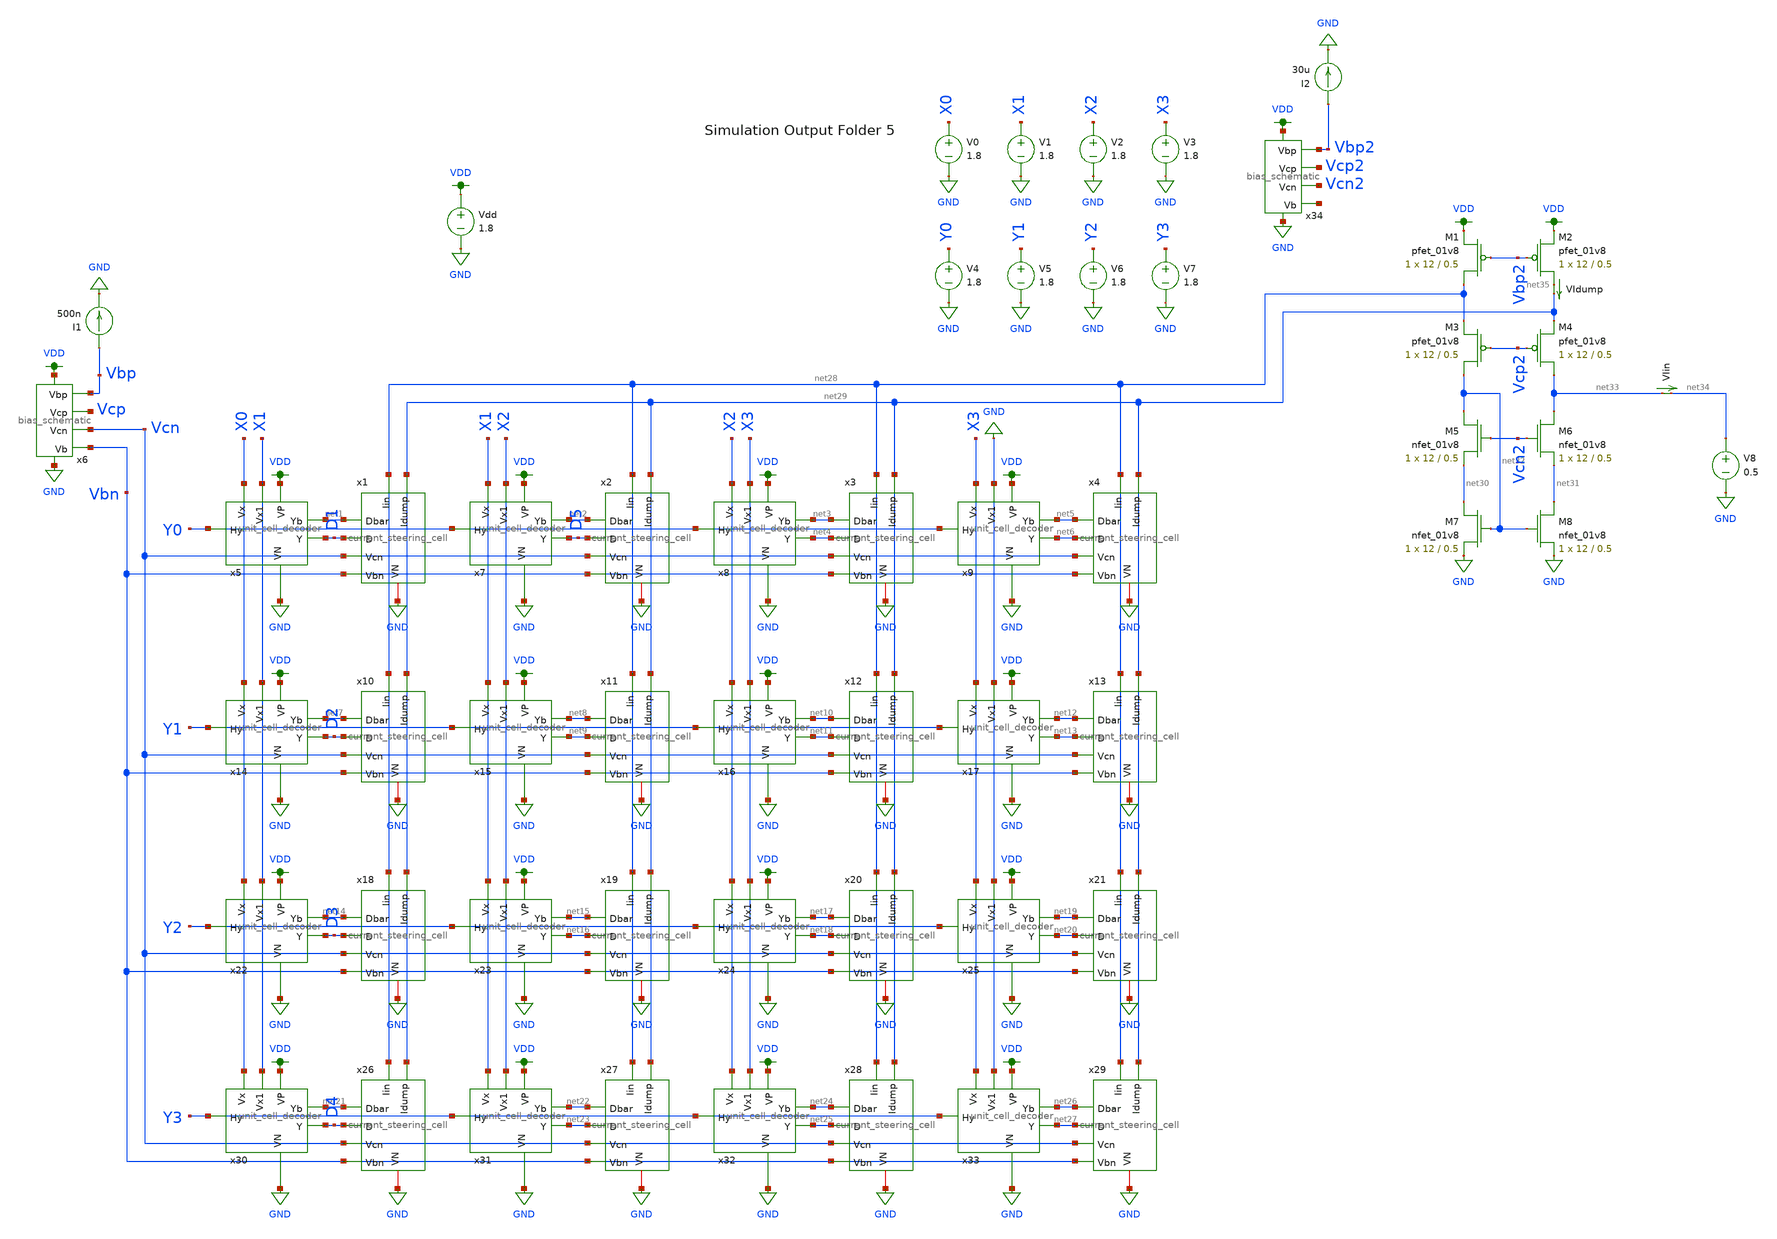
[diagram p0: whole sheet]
** sch_path: xschem/current_steering_testbenches/current_steering_testbench_current_difference.sch
**.subckt current_steering_testbench_current_difference
V1 X1 GND 1.8
V2 X2 GND 1.8
V3 X3 GND 1.8
V4 Y0 GND 1.8
I1 Vbp GND 500n
VIin net33 net34 0
.save i(viin)
Vdd VDD GND 1.8
XM1 net28 Vbp2 VDD VDD sky130_fd_pr__pfet_01v8 L=0.5 W=12 nf=1 ad='int((nf+1)/2) * W/nf * 0.29' as='int((nf+2)/2) * W/nf * 0.29'
+ pd='2*int((nf+1)/2) * (W/nf + 0.29)' ps='2*int((nf+2)/2) * (W/nf + 0.29)' nrd='0.29 / W' nrs='0.29 / W'
+ sa=0 sb=0 sd=0 mult=1 m=1
XM2 net35 Vbp2 VDD VDD sky130_fd_pr__pfet_01v8 L=0.5 W=12 nf=1 ad='int((nf+1)/2) * W/nf * 0.29' as='int((nf+2)/2) * W/nf * 0.29'
+ pd='2*int((nf+1)/2) * (W/nf + 0.29)' ps='2*int((nf+2)/2) * (W/nf + 0.29)' nrd='0.29 / W' nrs='0.29 / W'
+ sa=0 sb=0 sd=0 mult=1 m=1
XM3 net32 Vcp2 net28 VDD sky130_fd_pr__pfet_01v8 L=0.5 W=12 nf=1 ad='int((nf+1)/2) * W/nf * 0.29' as='int((nf+2)/2) * W/nf * 0.29'
+ pd='2*int((nf+1)/2) * (W/nf + 0.29)' ps='2*int((nf+2)/2) * (W/nf + 0.29)' nrd='0.29 / W' nrs='0.29 / W'
+ sa=0 sb=0 sd=0 mult=1 m=1
XM4 net33 Vcp2 net29 VDD sky130_fd_pr__pfet_01v8 L=0.5 W=12 nf=1 ad='int((nf+1)/2) * W/nf * 0.29' as='int((nf+2)/2) * W/nf * 0.29'
+ pd='2*int((nf+1)/2) * (W/nf + 0.29)' ps='2*int((nf+2)/2) * (W/nf + 0.29)' nrd='0.29 / W' nrs='0.29 / W'
+ sa=0 sb=0 sd=0 mult=1 m=1
V5 Y1 GND 1.8
V6 Y2 GND 1.8
V7 Y3 GND 1.8
V0 X0 GND 1.8
x5 X0 X1 Y0 VDD GND net1 D1 unit_cell_decoder
x7 X1 X2 Y0 VDD GND net2 D5 unit_cell_decoder
x8 X2 X3 Y0 VDD GND net3 net4 unit_cell_decoder
x9 X3 GND Y0 VDD GND net5 net6 unit_cell_decoder
x14 X0 X1 Y1 VDD GND net7 D2 unit_cell_decoder
x15 X1 X2 Y1 VDD GND net8 net9 unit_cell_decoder
x16 X2 X3 Y1 VDD GND net10 net11 unit_cell_decoder
x17 X3 GND Y1 VDD GND net12 net13 unit_cell_decoder
x22 X0 X1 Y2 VDD GND net14 D3 unit_cell_decoder
x23 X1 X2 Y2 VDD GND net15 net16 unit_cell_decoder
x24 X2 X3 Y2 VDD GND net17 net18 unit_cell_decoder
x25 X3 GND Y2 VDD GND net19 net20 unit_cell_decoder
x30 X0 X1 Y3 VDD GND net21 D4 unit_cell_decoder
x31 X1 X2 Y3 VDD GND net22 net23 unit_cell_decoder
x32 X2 X3 Y3 VDD GND net24 net25 unit_cell_decoder
x33 X3 GND Y3 VDD GND net26 net27 unit_cell_decoder
x1 net28 net29 net1 D1 Vcn Vbn GND current_steering_cell
x2 net28 net29 net2 D5 Vcn Vbn GND current_steering_cell
x3 net28 net29 net3 net4 Vcn Vbn GND current_steering_cell
x4 net28 net29 net5 net6 Vcn Vbn GND current_steering_cell
x10 net28 net29 net7 D2 Vcn Vbn GND current_steering_cell
x11 net28 net29 net8 net9 Vcn Vbn GND current_steering_cell
x12 net28 net29 net10 net11 Vcn Vbn GND current_steering_cell
x13 net28 net29 net12 net13 Vcn Vbn GND current_steering_cell
x18 net28 net29 net14 D3 Vcn Vbn GND current_steering_cell
x19 net28 net29 net15 net16 Vcn Vbn GND current_steering_cell
x20 net28 net29 net17 net18 Vcn Vbn GND current_steering_cell
x21 net28 net29 net19 net20 Vcn Vbn GND current_steering_cell
x26 net28 net29 net21 D4 Vcn Vbn GND current_steering_cell
x27 net28 net29 net22 net23 Vcn Vbn GND current_steering_cell
x28 net28 net29 net24 net25 Vcn Vbn GND current_steering_cell
x29 net28 net29 net26 net27 Vcn Vbn GND current_steering_cell
x6 VDD Vbp Vcp Vcn GND Vbn bias_schematic
XM5 net32 Vcn2 net30 GND sky130_fd_pr__nfet_01v8 L=0.5 W=12 nf=1 ad='int((nf+1)/2) * W/nf * 0.29' as='int((nf+2)/2) * W/nf * 0.29'
+ pd='2*int((nf+1)/2) * (W/nf + 0.29)' ps='2*int((nf+2)/2) * (W/nf + 0.29)' nrd='0.29 / W' nrs='0.29 / W'
+ sa=0 sb=0 sd=0 mult=1 m=1
XM6 net33 Vcn2 net31 GND sky130_fd_pr__nfet_01v8 L=0.5 W=12 nf=1 ad='int((nf+1)/2) * W/nf * 0.29' as='int((nf+2)/2) * W/nf * 0.29'
+ pd='2*int((nf+1)/2) * (W/nf + 0.29)' ps='2*int((nf+2)/2) * (W/nf + 0.29)' nrd='0.29 / W' nrs='0.29 / W'
+ sa=0 sb=0 sd=0 mult=1 m=1
XM7 net30 net32 GND GND sky130_fd_pr__nfet_01v8 L=0.5 W=12 nf=1 ad='int((nf+1)/2) * W/nf * 0.29' as='int((nf+2)/2) * W/nf * 0.29'
+ pd='2*int((nf+1)/2) * (W/nf + 0.29)' ps='2*int((nf+2)/2) * (W/nf + 0.29)' nrd='0.29 / W' nrs='0.29 / W'
+ sa=0 sb=0 sd=0 mult=1 m=1
XM8 net31 net32 GND GND sky130_fd_pr__nfet_01v8 L=0.5 W=12 nf=1 ad='int((nf+1)/2) * W/nf * 0.29' as='int((nf+2)/2) * W/nf * 0.29'
+ pd='2*int((nf+1)/2) * (W/nf + 0.29)' ps='2*int((nf+2)/2) * (W/nf + 0.29)' nrd='0.29 / W' nrs='0.29 / W'
+ sa=0 sb=0 sd=0 mult=1 m=1
V8 net34 GND 0.5
VIdump net35 net29 0
.save i(vidump)
I2 Vbp2 GND 30u
x34 VDD Vbp2 Vcp2 Vcn2 GND net36 bias_schematic
**** begin user architecture code

.save all
.control
set wr_vecnames
set wr_singlescale

let mc_runs = 1
let run = 1
dowhile run <= mc_runs

  let code = 0
  while code <= 16

    if code eq 0
      let y0 = 1 * 1.8
      let y1 = 1 * 1.8
      let y2 = 1 * 1.8
      let y3 = 1 * 1.8
      let x0 = 0 * 1.8
      let x1 = 0 * 1.8
      let x2 = 0 * 1.8
      let x3 = 0 * 1.8
    end
    if code eq 1
      let y0 = 1 * 1.8
      let y1 = 0 * 1.8
      let y2 = 0 * 1.8
      let y3 = 0 * 1.8
      let x0 = 1 * 1.8
      let x1 = 0 * 1.8
      let x2 = 0 * 1.8
      let x3 = 0 * 1.8
    end
    if code eq 2
      let y0 = 1 * 1.8
      let y1 = 1 * 1.8
      let y2 = 0 * 1.8
      let y3 = 0 * 1.8
      let x0 = 1 * 1.8
      let x1 = 0 * 1.8
      let x2 = 0 * 1.8
      let x3 = 0 * 1.8
    end
    if code eq 3
      let y0 = 1 * 1.8
      let y1 = 1 * 1.8
      let y2 = 1 * 1.8
      let y3 = 0 * 1.8
      let x0 = 1 * 1.8
      let x1 = 0 * 1.8
      let x2 = 0 * 1.8
      let x3 = 0 * 1.8
    end
    if code eq 4
      let y0 = 1 * 1.8
      let y1 = 1 * 1.8
      let y2 = 1 * 1.8
      let y3 = 1 * 1.8
      let x0 = 1 * 1.8
      let x1 = 0 * 1.8
      let x2 = 0 * 1.8
      let x3 = 0 * 1.8
    end
    if code eq 5
      let y0 = 1 * 1.8
      let y1 = 0 * 1.8
      let y2 = 0 * 1.8
      let y3 = 0 * 1.8
      let x0 = 1 * 1.8
      let x1 = 1 * 1.8
      let x2 = 0 * 1.8
      let x3 = 0 * 1.8
    end
    if code eq 6
      let y0 = 1 * 1.8
      let y1 = 1 * 1.8
      let y2 = 0 * 1.8
      let y3 = 0 * 1.8
      let x0 = 1 * 1.8
      let x1 = 1 * 1.8
      let x2 = 0 * 1.8
      let x3 = 0 * 1.8
    end
    if code eq 7
      let y0 = 1 * 1.8
      let y1 = 1 * 1.8
      let y2 = 1 * 1.8
      let y3 = 0 * 1.8
      let x0 = 1 * 1.8
      let x1 = 1 * 1.8
      let x2 = 0 * 1.8
      let x3 = 0 * 1.8
    end
    if code eq 8
      let y0 = 1 * 1.8
      let y1 = 1 * 1.8
      let y2 = 1 * 1.8
      let y3 = 1 * 1.8
      let x0 = 1 * 1.8
      let x1 = 1 * 1.8
      let x2 = 0 * 1.8
      let x3 = 0 * 1.8
    end
    if code eq 9
      let y0 = 1 * 1.8
      let y1 = 0 * 1.8
      let y2 = 0 * 1.8
      let y3 = 0 * 1.8
      let x0 = 1 * 1.8
      let x1 = 1 * 1.8
      let x2 = 1 * 1.8
      let x3 = 0 * 1.8
    end
    if code eq 10
      let y0 = 1 * 1.8
      let y1 = 1 * 1.8
      let y2 = 0 * 1.8
      let y3 = 0 * 1.8
      let x0 = 1 * 1.8
      let x1 = 1 * 1.8
      let x2 = 1 * 1.8
      let x3 = 0 * 1.8
    end
    if code eq 11
      let y0 = 1 * 1.8
      let y1 = 1 * 1.8
      let y2 = 1 * 1.8
      let y3 = 0 * 1.8
      let x0 = 1 * 1.8
      let x1 = 1 * 1.8
      let x2 = 1 * 1.8
      let x3 = 0 * 1.8
    end
    if code eq 12
      let y0 = 1 * 1.8
      let y1 = 1 * 1.8
      let y2 = 1 * 1.8
      let y3 = 1 * 1.8
      let x0 = 1 * 1.8
      let x1 = 1 * 1.8
      let x2 = 1 * 1.8
      let x3 = 0 * 1.8
    end
    if code eq 13
      let y0 = 1 * 1.8
      let y1 = 0 * 1.8
      let y2 = 0 * 1.8
      let y3 = 0 * 1.8
      let x0 = 1 * 1.8
      let x1 = 1 * 1.8
      let x2 = 1 * 1.8
      let x3 = 1 * 1.8
    end
    if code eq 14
      let y0 = 1 * 1.8
      let y1 = 1 * 1.8
      let y2 = 0 * 1.8
      let y3 = 0 * 1.8
      let x0 = 1 * 1.8
      let x1 = 1 * 1.8
      let x2 = 1 * 1.8
      let x3 = 1 * 1.8
    end
    if code eq 15
      let y0 = 1 * 1.8
      let y1 = 1 * 1.8
      let y2 = 1 * 1.8
      let y3 = 0 * 1.8
      let x0 = 1 * 1.8
      let x1 = 1 * 1.8
      let x2 = 1 * 1.8
      let x3 = 1 * 1.8
    end
    if code eq 16
      let y0 = 1 * 1.8
      let y1 = 1 * 1.8
      let y2 = 1 * 1.8
      let y3 = 1 * 1.8
      let x0 = 1 * 1.8
      let x1 = 1 * 1.8
      let x2 = 1 * 1.8
      let x3 = 1 * 1.8
    end

    alter V0 $&x0
    alter V1 $&x1
    alter V2 $&x2
    alter V3 $&x3
    alter V4 $&y0
    alter V5 $&y1
    alter V6 $&y2
    alter V7 $&y3


    save all
    op

    wrdata ~/dev/git/magic-dds/simulations/current_steering_dac/5/ieeeDAC_{$&run}.txt code v(D1) v(D2)
+ v(D3) v(D4) v(D5) i(VIin) i(VIdump)
    if code eq 0
      set appendwrite
      set wr_vecnames = FALSE
    end
    let code = code + 1
  end
  reset
  set appendwrite = FALSE
  set wr_vecnames
  let run = run + 1
end
.endc


.option wnflag=1
.param MC_SWITCH=0.0
.lib ~/skywater/skywater-pdk/libraries/sky130_fd_pr_ngspice/latest/models/sky130.lib.spice tt

**** end user architecture code
**.ends
.GLOBAL GND
.GLOBAL VDD
.end
